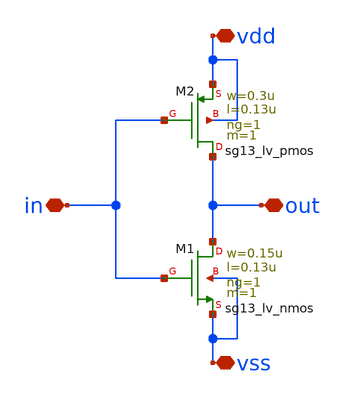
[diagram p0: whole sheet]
** sch_path: design/blocks/inverter/schematic/inverter.sch
**.subckt inverter vdd vss out in
*.iopin vdd
*.iopin vss
*.iopin out
*.iopin in
XM2 out in vdd vdd sg13_lv_pmos w=0.3u l=0.13u ng=1 m=1 mm_ok=1
XM1 out in vss vss sg13_lv_nmos w=0.15u l=0.13u ng=1 m=1 mm_ok=1
**.ends
.end
